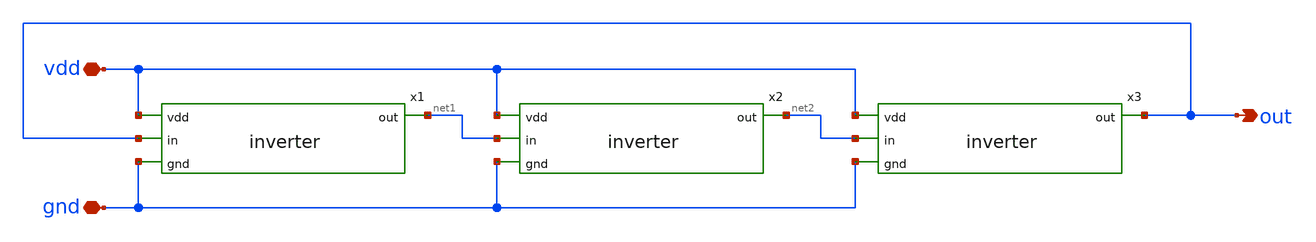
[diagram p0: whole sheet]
** sch_path: oscillator/oscillator.sch
**.subckt oscillator vdd gnd out
*.iopin vdd
*.iopin gnd
*.opin out
x1 vdd out net1 gnd inverter
x2 vdd net1 net2 gnd inverter
x3 vdd net2 out gnd inverter
**.ends

* expanding   symbol:  inverter.sym # of pins=4
** sym_path: oscillator/inverter.sym
** sch_path: oscillator/inverter.sch
.subckt inverter vdd in out gnd
*.ipin vdd
*.ipin in
*.ipin gnd
*.opin out
XM1 out in vdd vdd sky130_fd_pr__pfet_01v8 L=0.15 W=1 nf=1 ad='int((nf+1)/2) * W/nf * 0.29' as='int((nf+2)/2) * W/nf * 0.29'
+ pd='2*int((nf+1)/2) * (W/nf + 0.29)' ps='2*int((nf+2)/2) * (W/nf + 0.29)' nrd='0.29 / W' nrs='0.29 / W'
+ sa=0 sb=0 sd=0 mult=1 m=1
XM2 out in gnd gnd sky130_fd_pr__nfet_01v8 L=0.15 W=1 nf=1 ad='int((nf+1)/2) * W/nf * 0.29' as='int((nf+2)/2) * W/nf * 0.29'
+ pd='2*int((nf+1)/2) * (W/nf + 0.29)' ps='2*int((nf+2)/2) * (W/nf + 0.29)' nrd='0.29 / W' nrs='0.29 / W'
+ sa=0 sb=0 sd=0 mult=1 m=1
.ends

.end
